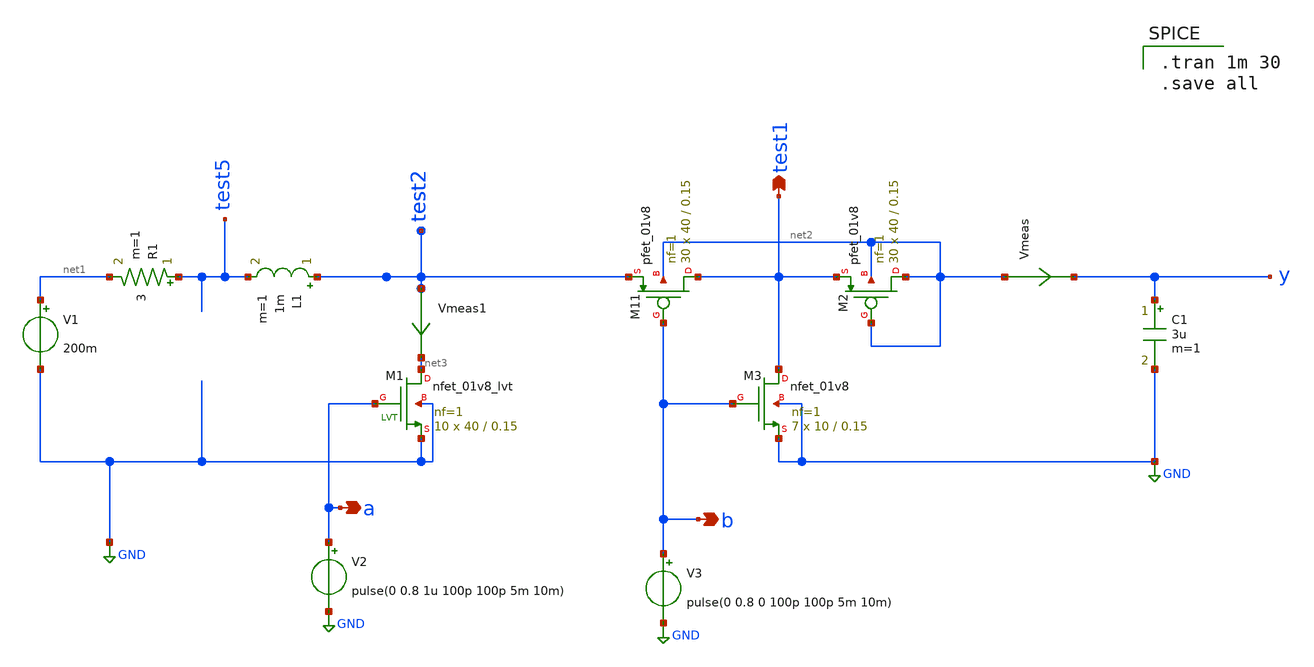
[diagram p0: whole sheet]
** sch_path: component/Core Functionality of boost Converter/vs test_l.sch
**.subckt vs test_l a test1 b
*.opin a
*.opin test1
*.opin b
V1 net1 GND 200m
C1 y GND 3u m=1
L1 test2 test5 1m m=1
XM11 test1 b test2 net2 sky130_fd_pr__pfet_01v8 L=0.15 W=40 nf=1 ad='int((nf+1)/2) * W/nf * 0.29' as='int((nf+2)/2) * W/nf * 0.29'
+ pd='2*int((nf+1)/2) * (W/nf + 0.29)' ps='2*int((nf+2)/2) * (W/nf + 0.29)' nrd='0.29 / W' nrs='0.29 / W'
+ sa=0 sb=0 sd=0 mult=30 m=30
V2 a GND pulse(0 0.8 1u 100p 100p 5m 10m)
Vmeas net2 y 0
.save i(vmeas)
Vmeas1 test2 net3 0
.save i(vmeas1)
XM2 net2 net2 test1 net2 sky130_fd_pr__pfet_01v8 L=0.15 W=40 nf=1 ad='int((nf+1)/2) * W/nf * 0.29' as='int((nf+2)/2) * W/nf * 0.29'
+ pd='2*int((nf+1)/2) * (W/nf + 0.29)' ps='2*int((nf+2)/2) * (W/nf + 0.29)' nrd='0.29 / W' nrs='0.29 / W'
+ sa=0 sb=0 sd=0 mult=30 m=30
XM3 test1 b GND GND sky130_fd_pr__nfet_01v8 L=0.15 W=10 nf=1 ad='int((nf+1)/2) * W/nf * 0.29' as='int((nf+2)/2) * W/nf * 0.29'
+ pd='2*int((nf+1)/2) * (W/nf + 0.29)' ps='2*int((nf+2)/2) * (W/nf + 0.29)' nrd='0.29 / W' nrs='0.29 / W'
+ sa=0 sb=0 sd=0 mult=7 m=7
V3 b GND pulse(0 0.8 0 100p 100p 5m 10m)
XM1 net3 a GND GND sky130_fd_pr__nfet_01v8_lvt L=0.15 W=40 nf=1 ad='int((nf+1)/2) * W/nf * 0.29' as='int((nf+2)/2) * W/nf * 0.29'
+ pd='2*int((nf+1)/2) * (W/nf + 0.29)' ps='2*int((nf+2)/2) * (W/nf + 0.29)' nrd='0.29 / W' nrs='0.29 / W'
+ sa=0 sb=0 sd=0 mult=10 m=10
R1 test5 net1 3 m=1
**** begin user architecture code

** opencircuitdesign pdks install
.lib $::SKYWATER_MODELS/sky130.lib.spice tt



.tran 1m 30
.save all

**** end user architecture code
**.ends
.GLOBAL GND
.end
